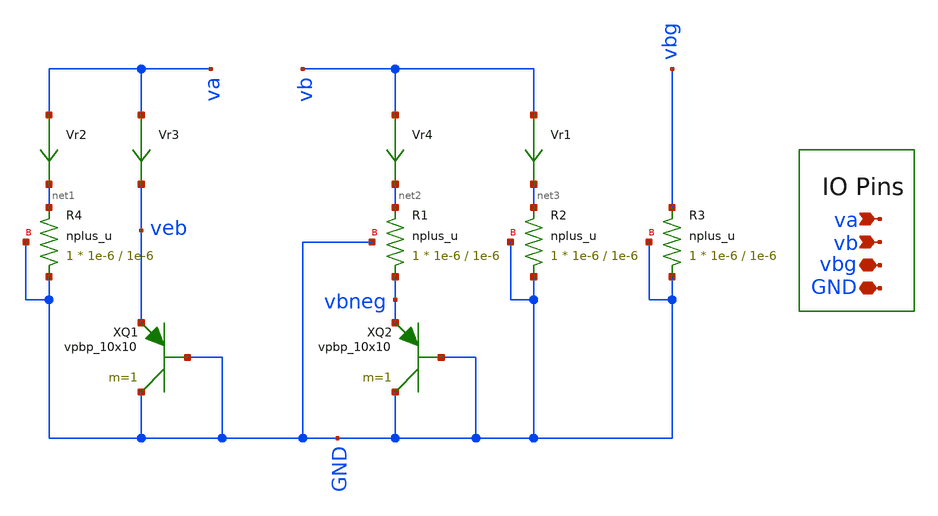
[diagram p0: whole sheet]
** sch_path: gf180_bandcapCore-ckt.sch
**.subckt gf180_bandcapCore-ckt va vb vbg GND
*.ipin va
*.ipin vb
*.iopin vbg
*.iopin GND
XQ1 GND GND veb vpbp_10x10 m=1
XQ2 GND GND vbneg vpbp_10x10 m=1
XR1 vbneg net2 GND nplus_u r_width=1e-6 r_length=1e-6 m=1
XR2 GND net3 GND nplus_u r_width=1e-6 r_length=1e-6 m=1
XR3 GND vbg GND nplus_u r_width=1e-6 r_length=1e-6 m=1
XR4 GND net1 GND nplus_u r_width=1e-6 r_length=1e-6 m=1
Vr4 vb net2 0
.save i(vr4)
Vr1 vb net3 0
.save i(vr1)
Vr2 va net1 0
.save i(vr2)
Vr3 va veb 0
.save i(vr3)
**.ends
.end
